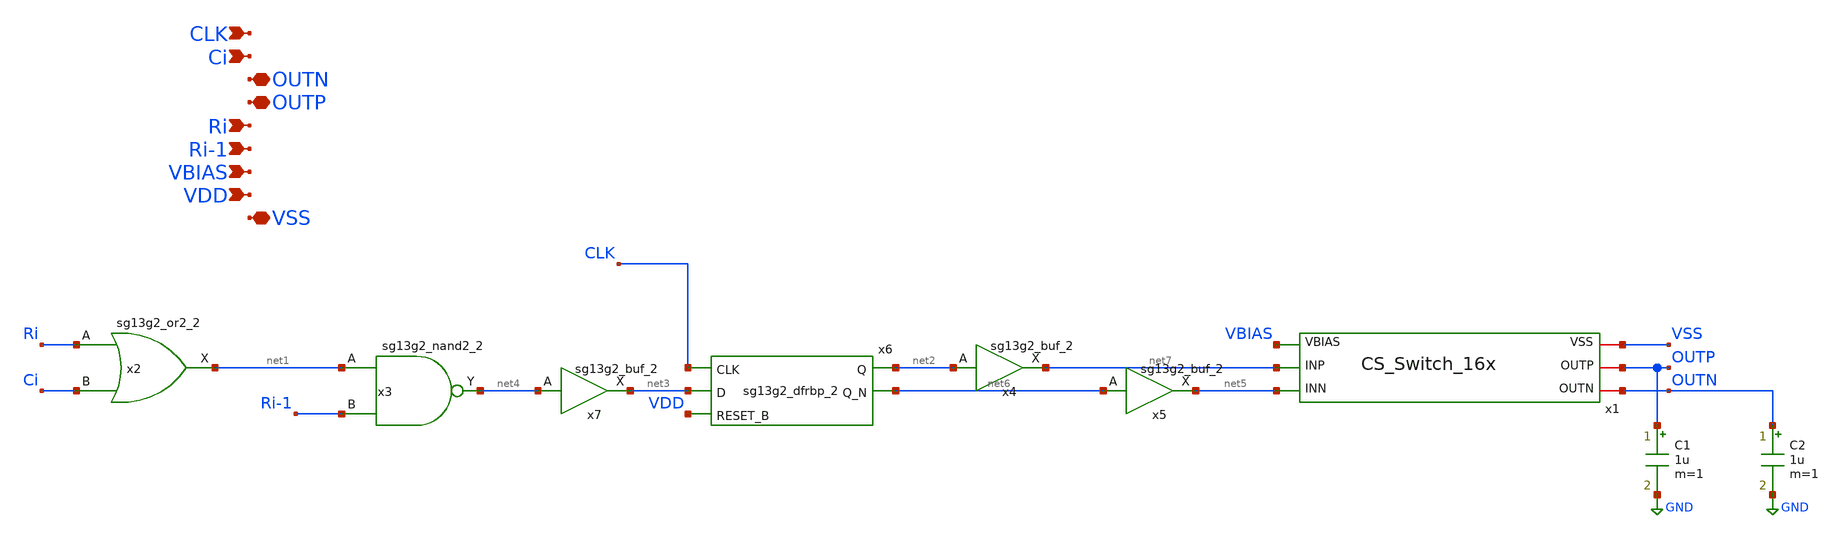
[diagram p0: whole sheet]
** sch_path: klayout/xschem/Unit_cell.sch
* IHP-GmbH/IHP-Open-PDK/ihp-sg13g2/libs.tech/xschem/sg13g2_stdcells/sg13g2_or2_2.sch:
* Copyright 2023 IHP PDK Authors
* Licensed under the Apache License, Version 2.0 (the "License");
**.subckt Unit_cell VSS VDD VBIAS Ri-1 Ri OUTP OUTN Ci CLK
*.iopin VSS
*.ipin VDD
*.ipin VBIAS
*.ipin Ri-1
*.ipin Ri
*.iopin OUTP
*.iopin OUTN
*.ipin Ci
*.ipin CLK
x1 net5 net7 OUTN OUTP VBIAS VSS CS_Switch_16x
x2 net1 Ri Ci VDD VSS sg13g2_or2_2
x3 net4 net1 Ri-1 VDD VSS sg13g2_nand2_2
x6 net2 net6 CLK net3 VDD VDD VSS sg13g2_dfrbp_2
C1 OUTP GND 1u m=1
C2 OUTN GND 1u m=1
x4 net7 net2 VDD VSS sg13g2_buf_2
x5 net5 net6 VDD VSS sg13g2_buf_2
x7 net3 net4 VDD VSS sg13g2_buf_2
**.ends

* expanding   symbol:  CS_Switch_16x.sym # of pins=6
** sym_path: CS_Switch_16x.sym
** sch_path: CS_Switch_16x.sch
.subckt CS_Switch_16x INN INP OUTN OUTP VBIAS VSS
*.iopin VSS
*.ipin VBIAS
*.iopin OUTP
*.iopin OUTN
*.ipin INP
*.ipin INN
XM1 OUTP INP net1 VSS sg13_lv_nmos w=1u l=0.13u ng=1 m=1 mm_ok=1
XM2 OUTP INP net1 VSS sg13_lv_nmos w=1u l=0.13u ng=1 m=1 mm_ok=1
XM3 OUTN INN net1 VSS sg13_lv_nmos w=1u l=0.13u ng=1 m=1 mm_ok=1
XM4 OUTN INN net1 VSS sg13_lv_nmos w=1u l=0.13u ng=1 m=1 mm_ok=1
XM7 net1 VBIAS net2 VSS sg13_hv_nmos w=5.2u l=0.45u ng=1 m=1 mm_ok=1
XM5 net2 VBIAS VSS VSS sg13_hv_nmos w=5.2u l=0.45u ng=1 m=1 mm_ok=1
C2 net1 GND 1u m=1
.ends


* expanding   symbol:  sg13g2_stdcells/sg13g2_or2_2.sym # of pins=3
** sym_path: sg13g2_stdcells/sg13g2_or2_2.sym
** sch_path: sg13g2_stdcells/sg13g2_or2_2.sch
.subckt sg13g2_or2_2 X A B VDD VSS
*.opin X
*.ipin B
*.ipin A
*.iopin VDD
*.iopin VSS
XM1 net1 B VSS VSS sg13_lv_nmos w=550.00n l=130.00n ng=1 m=1 mm_ok=1
XM2 net1 A VSS VSS sg13_lv_nmos w=550.00n l=130.00n ng=1 m=1 mm_ok=1
XM3 X net1 VSS VSS sg13_lv_nmos w=1.48u l=130.00n ng=2 m=1 mm_ok=1
XM4 net2 A VDD VDD sg13_lv_pmos w=840.00n l=130.00n ng=1 m=1 mm_ok=1
XM5 net1 B net2 VDD sg13_lv_pmos w=840.00n l=130.00n ng=1 m=1 mm_ok=1
XM6 X net1 VDD VDD sg13_lv_pmos w=2.24u l=130.00n ng=2 m=1 mm_ok=1
.ends


* expanding   symbol:  sg13g2_stdcells/sg13g2_nand2_2.sym # of pins=3
** sym_path: sg13g2_stdcells/sg13g2_nand2_2.sym
** sch_path: sg13g2_stdcells/sg13g2_nand2_2.sch
.subckt sg13g2_nand2_2 Y A B VDD VSS
*.iopin VDD
*.iopin VSS
*.opin Y
*.ipin B
*.ipin A
XM1 Y A net1 VSS sg13_lv_nmos w=1.44u l=130.00n ng=2 m=1 mm_ok=1
XM2 net1 B VSS VSS sg13_lv_nmos w=1.44u l=130.00n ng=2 m=1 mm_ok=1
XM3 Y A VDD VDD sg13_lv_pmos w=2.24u l=130.00n ng=2 m=1 mm_ok=1
XM4 Y B VDD VDD sg13_lv_pmos w=2.24u l=130.00n ng=2 m=1 mm_ok=1
.ends


* expanding   symbol:  sg13g2_stdcells/sg13g2_dfrbp_2.sym # of pins=5
** sym_path: sg13g2_stdcells/sg13g2_dfrbp_2.sym
** sch_path: sg13g2_stdcells/sg13g2_dfrbp_2.sch
.subckt sg13g2_dfrbp_2 Q Q_N CLK D RESET_B VDD VSS
*.ipin D
*.ipin RESET_B
*.ipin CLK
*.opin Q
*.opin Q_N
*.iopin VDD
*.iopin VSS
XM1 Db D net12 VSS sg13_lv_nmos w=420.00n l=130.00n ng=1 m=1 mm_ok=1
XM2 net12 RESET_B VSS VSS sg13_lv_nmos w=420.00n l=130.00n ng=1 m=1 mm_ok=1
XM3 net2 clkneg net11 VSS sg13_lv_nmos w=420.00n l=130.00n ng=1 m=1 mm_ok=1
XM4 net11 net3 VSS VSS sg13_lv_nmos w=420.00n l=130.00n ng=1 m=1 mm_ok=1
XM5 net3 net2 net7 VSS sg13_lv_nmos w=420.00n l=130.00n ng=1 m=1 mm_ok=1
XM6 net7 RESET_B VSS VSS sg13_lv_nmos w=420.00n l=130.00n ng=1 m=1 mm_ok=1
XM7 Q_N net2 VSS VSS sg13_lv_nmos w=1.48u l=130.00n ng=2 m=1 mm_ok=1
XM8 net1 net2 VSS VSS sg13_lv_nmos w=640.00n l=130.00n ng=1 m=1 mm_ok=1
XM9 Q net1 VSS VSS sg13_lv_nmos w=1.48u l=130.00n ng=2 m=1 mm_ok=1
XM10 clkneg CLK VSS VSS sg13_lv_nmos w=740.00n l=130.00n ng=1 m=1 mm_ok=1
XM11 clkpos clkneg VSS VSS sg13_lv_nmos w=740.00n l=130.00n ng=1 m=1 mm_ok=1
XM12 Db clkneg net4 VSS sg13_lv_nmos w=420.00n l=130.00n ng=1 m=1 mm_ok=1
XM13 net4 clkpos net10 VSS sg13_lv_nmos w=420.00n l=130.00n ng=1 m=1 mm_ok=1
XM14 net10 net5 net6 VSS sg13_lv_nmos w=420.00n l=130.00n ng=1 m=1 mm_ok=1
XM15 net6 RESET_B VSS VSS sg13_lv_nmos w=420.00n l=130.00n ng=1 m=1 mm_ok=1
XM16 net5 net4 VSS VSS sg13_lv_nmos w=740.00n l=130.00n ng=1 m=1 mm_ok=1
XM17 net5 clkpos net2 VSS sg13_lv_nmos w=740.00n l=130.00n ng=1 m=1 mm_ok=1
XM18 Db RESET_B VDD VDD sg13_lv_pmos w=420.00n l=130.00n ng=1 m=1 mm_ok=1
XM19 Db D VDD VDD sg13_lv_pmos w=420.00n l=130.00n ng=1 m=1 mm_ok=1
XM20 net9 net3 VDD VDD sg13_lv_pmos w=420.00n l=130.00n ng=1 m=1 mm_ok=1
XM21 net2 clkpos net9 VDD sg13_lv_pmos w=420.00n l=130.00n ng=1 m=1 mm_ok=1
XM22 net3 net2 VDD VDD sg13_lv_pmos w=420.00n l=130.00n ng=1 m=1 mm_ok=1
XM23 net3 RESET_B VDD VDD sg13_lv_pmos w=420.00n l=130.00n ng=1 m=1 mm_ok=1
XM24 Q_N net2 VDD VDD sg13_lv_pmos w=2.24u l=130.00n ng=2 m=1 mm_ok=1
XM25 net1 net2 VDD VDD sg13_lv_pmos w=1.000u l=130.00n ng=1 m=1 mm_ok=1
XM26 Q net1 VDD VDD sg13_lv_pmos w=2.24u l=130.00n ng=2 m=1 mm_ok=1
XM27 clkneg CLK VDD VDD sg13_lv_pmos w=1.12u l=130.00n ng=1 m=1 mm_ok=1
XM28 clkpos clkneg VDD VDD sg13_lv_pmos w=1.12u l=130.00n ng=1 m=1 mm_ok=1
XM29 Db clkpos net4 VDD sg13_lv_pmos w=420.00n l=130.00n ng=1 m=1 mm_ok=1
XM30 net8 net5 VDD VDD sg13_lv_pmos w=420.00n l=130.00n ng=1 m=1 mm_ok=1
XM31 net4 clkneg net8 VDD sg13_lv_pmos w=420.00n l=130.00n ng=1 m=1 mm_ok=1
XM32 net4 RESET_B VDD VDD sg13_lv_pmos w=420.00n l=130.00n ng=1 m=1 mm_ok=1
XM33 net5 net4 VDD VDD sg13_lv_pmos w=1.000u l=130.00n ng=1 m=1 mm_ok=1
XM34 net5 clkneg net2 VDD sg13_lv_pmos w=1.000u l=130.00n ng=1 m=1 mm_ok=1
.ends


* expanding   symbol:  sg13g2_stdcells/sg13g2_buf_2.sym # of pins=2
** sym_path: sg13g2_stdcells/sg13g2_buf_2.sym
** sch_path: sg13g2_stdcells/sg13g2_buf_2.sch
.subckt sg13g2_buf_2 X A VDD VSS
*.ipin A
*.opin X
*.iopin VDD
*.iopin VSS
XM1 net1 A VSS VSS sg13_lv_nmos w=640.00n l=130.00n ng=1 m=1 mm_ok=1
XM2 X net1 VSS VSS sg13_lv_nmos w=1.48u l=130.00n ng=2 m=1 mm_ok=1
XM3 net1 A VDD VDD sg13_lv_pmos w=1.000u l=130.00n ng=1 m=1 mm_ok=1
XM4 X net1 VDD VDD sg13_lv_pmos w=2.24u l=130.00n ng=2 m=1 mm_ok=1
.ends

.GLOBAL GND
.end
